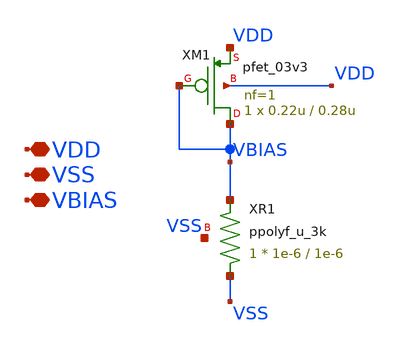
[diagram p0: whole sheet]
** sch_path: designs/libs/core_current-mirror/pbias-gen/pbias-gen.sch
**.subckt pbias-gen VDD VSS VBIAS
*.iopin VDD
*.iopin VSS
*.iopin VBIAS
XR1 VSS VBIAS VSS ppolyf_u_3k r_width=1e-6 r_length=1e-6 m=1
XM1 VBIAS VBIAS VDD VDD pfet_03v3 L=0.28u W=0.22u nf=1 ad='int((nf+1)/2) * W/nf * 0.18u' as='int((nf+2)/2) * W/nf * 0.18u'
+ pd='2*int((nf+1)/2) * (W/nf + 0.18u)' ps='2*int((nf+2)/2) * (W/nf + 0.18u)' nrd='0.18u / W' nrs='0.18u / W'
+ sa=0 sb=0 sd=0 m=1
**.ends
.end
